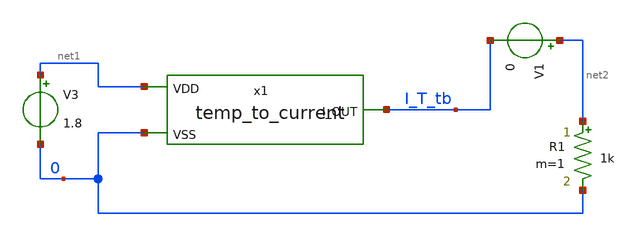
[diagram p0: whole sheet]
** sch_path: design/JNW_GR07_SKY130A/temp_to_current_tb.sch
**.subckt temp_to_current_tb
x1 net1 I_T_tb 0 temp_to_current
V3 net1 0 1.8
R1 net2 0 1k m=1
V1 net2 I_T_tb 0
**.ends
.end
